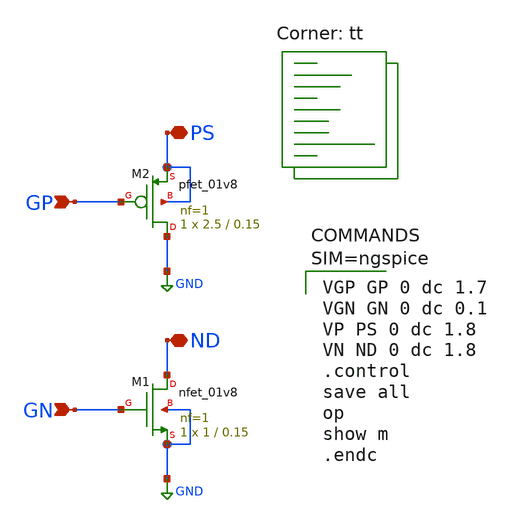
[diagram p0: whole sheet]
** sch_path: opbench.sch
**.subckt opbench GN ND PS GP
*.ipin GN
*.iopin ND
*.iopin PS
*.ipin GP
XM1 ND GN GND GND sky130_fd_pr__nfet_01v8 L=0.15 W=1 nf=1 ad='int((nf+1)/2) * W/nf * 0.29' as='int((nf+2)/2) * W/nf * 0.29'
+ pd='2*int((nf+1)/2) * (W/nf + 0.29)' ps='2*int((nf+2)/2) * (W/nf + 0.29)' nrd='0.29 / W' nrs='0.29 / W'
+ sa=0 sb=0 sd=0 mult=1 m=1
XM2 GND GP PS PS sky130_fd_pr__pfet_01v8 L=0.15 W=2.5 nf=1 ad='int((nf+1)/2) * W/nf * 0.29' as='int((nf+2)/2) * W/nf * 0.29'
+ pd='2*int((nf+1)/2) * (W/nf + 0.29)' ps='2*int((nf+2)/2) * (W/nf + 0.29)' nrd='0.29 / W' nrs='0.29 / W'
+ sa=0 sb=0 sd=0 mult=1 m=1
**** begin user architecture code
.lib $::SKYWATER_MODELS/sky130.lib.spice tt


VGP GP 0 dc 1.7
VGN GN 0 dc 0.1
VP PS 0 dc 1.8
VN ND 0 dc 1.8
.control
save all
op
show m
.endc


**** end user architecture code
**.ends
.GLOBAL GND
.end
